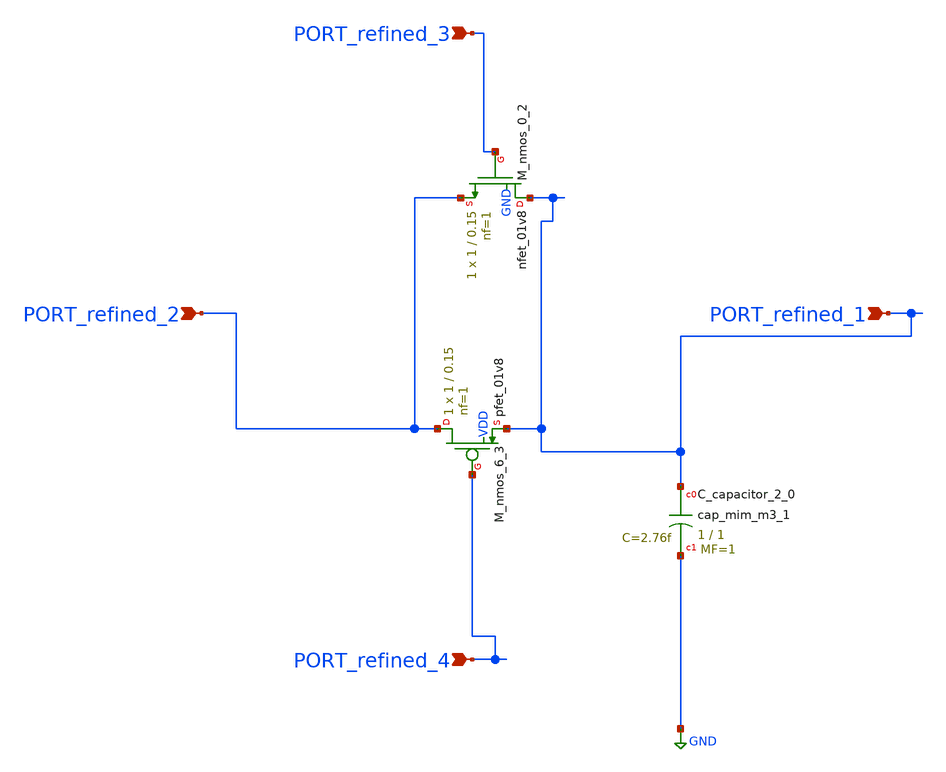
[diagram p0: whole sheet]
** sch_path: schematics/AMSNet/786.sch
**.subckt 786 PORT_refined_2 PORT_refined_1 PORT_refined_3 PORT_refined_4
*.ipin PORT_refined_2
*.ipin PORT_refined_1
*.ipin PORT_refined_3
*.ipin PORT_refined_4
XC_capacitor_2_0 PORT_refined_1 GND sky130_fd_pr__cap_mim_m3_1 W=1 L=1 MF=1 m=1
XM_nmos_0_2 PORT_refined_1 PORT_refined_3 PORT_refined_2 GND sky130_fd_pr__nfet_01v8 L=0.15 W=1 nf=1
+ ad='int((1 + 1)/2) * 1 / 1 * 0.29' as='int((1 + 2)/2) * 1 / 1 * 0.29' pd='2*int((1 + 1)/2) * (1 / 1 + 0.29)'
+ ps='2*int((1 + 2)/2) * (1 / 1 + 0.29)' nrd='0.29 / 1 ' nrs='0.29 / 1 ' sa=0 sb=0 sd=0 mult=1 m=1
XM_nmos_6_3 PORT_refined_2 PORT_refined_4 PORT_refined_1 VDD sky130_fd_pr__pfet_01v8 L=0.15 W=1 nf=1
+ ad='int((1 + 1)/2) * 1 / 1 * 0.29' as='int((1 + 2)/2) * 1 / 1 * 0.29' pd='2*int((1 + 1)/2) * (1 / 1 + 0.29)'
+ ps='2*int((1 + 2)/2) * (1 / 1 + 0.29)' nrd='0.29 / 1 ' nrs='0.29 / 1 ' sa=0 sb=0 sd=0 mult=1 m=1
**.ends
.GLOBAL GND
.end
